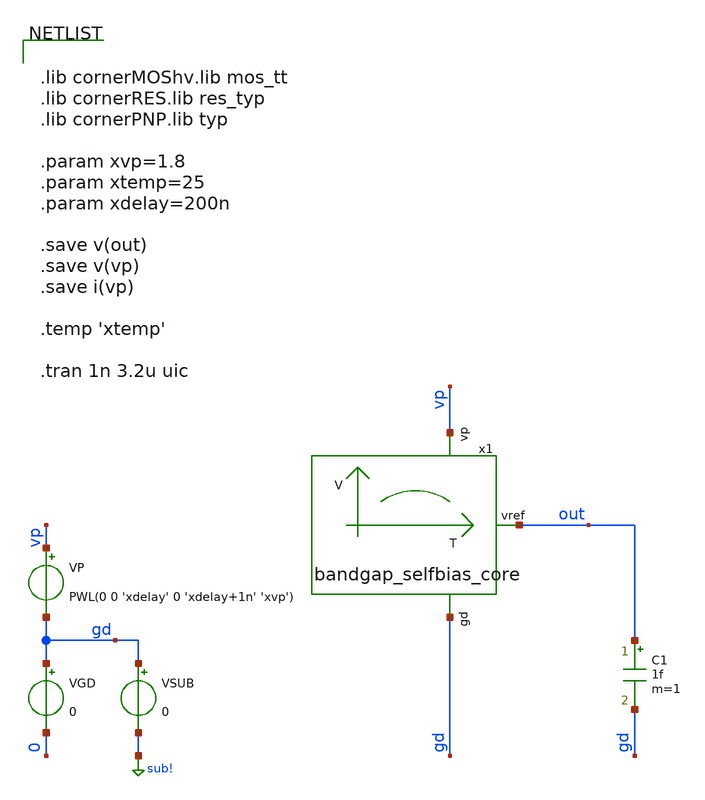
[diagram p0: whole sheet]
** sch_path: testbench/bandgap_selfbias_startup_tb.sch
**.subckt bandgap_selfbias_startup_tb
VGD gd 0 0
VSUB gd sub! 0
VP vp gd PWL(0 0 'xdelay' 0 'xdelay+1n' 'xvp')
C1 out gd 1f m=1
x1 vp out gd bandgap_selfbias_core
**** begin user architecture code


.lib cornerMOShv.lib mos_tt
.lib cornerRES.lib res_typ
.lib cornerPNP.lib typ

.param xvp=1.8
.param xtemp=25
.param xdelay=200n

.save v(out)
.save v(vp)
.save i(vp)

.temp 'xtemp'

.tran 1n 3.2u uic


**** end user architecture code
**.ends

* expanding   symbol:  /foss/designs/test/circuit/bandgap_selfbias_core.sym # of pins=3
** sym_path: /foss/designs/test/circuit/bandgap_selfbias_core.sym
** sch_path: /foss/designs/test/circuit/bandgap_selfbias_core.sch
.subckt bandgap_selfbias_core vp vref gd
*.ipin gd
*.ipin vp
*.opin vref
XM1 net1 net1 gd gd sg13_hv_nmos w=1.2u l=0.9u ng=1 m=2 mm_ok=1
XM2 net4 net1 net5 gd sg13_hv_nmos w=1.2u l=0.9u ng=1 m=8 mm_ok=1
XM7 net5 vref gd gd sg13_hv_nmos w=1.2u l=0.9u ng=1 m=4 mm_ok=1
XM3 net2 net2 net1 gd sg13_hv_nmos w=1.2u l=0.9u ng=1 m=2 mm_ok=1
XM4 net3 net2 net4 gd sg13_hv_nmos w=1.2u l=0.9u ng=1 m=8 mm_ok=1
XM6 net3 net3 vp vp sg13_hv_pmos w=1.2u l=0.9u ng=1 m=2 mm_ok=1
XM5 net2 net3 vp vp sg13_hv_pmos w=1.2u l=0.9u ng=1 m=2 mm_ok=1
XM10 net6 net3 vp vp sg13_hv_pmos w=1.2u l=0.9u ng=1 m=2 mm_ok=1
XM8 net7 net6 gd gd sg13_hv_nmos w=1.2u l=0.9u ng=1 m=20 mm_ok=1
XM9 net6 net6 net7 gd sg13_hv_nmos w=1.2u l=0.9u ng=1 m=12 mm_ok=1
XM13 net8 net3 vp vp sg13_hv_pmos w=1.2u l=0.9u ng=1 m=2 mm_ok=1
XM11 net9 net8 net7 gd sg13_hv_nmos w=1.2u l=0.9u ng=1 m=20 mm_ok=1
XM12 net8 net8 net9 gd sg13_hv_nmos w=1.2u l=0.9u ng=1 m=10 mm_ok=1
XM14 vref vref net9 gd sg13_hv_nmos w=1.2u l=0.9u ng=1 m=8 mm_ok=1
XM15 vref net3 vp vp sg13_hv_pmos w=1.2u l=0.9u ng=1 m=2 mm_ok=1
XM16 stup net2 gd gd sg13_hv_nmos w=1.2u l=0.9u ng=1 m=2 mm_ok=1
XM17 stup gd vp vp sg13_hv_pmos w=1.2u l=4.0u ng=1 m=1 mm_ok=1
XM18 net3 stup gd gd sg13_hv_nmos w=1.2u l=0.9u ng=1 m=2 mm_ok=1
.ends

.GLOBAL sub!
.end
